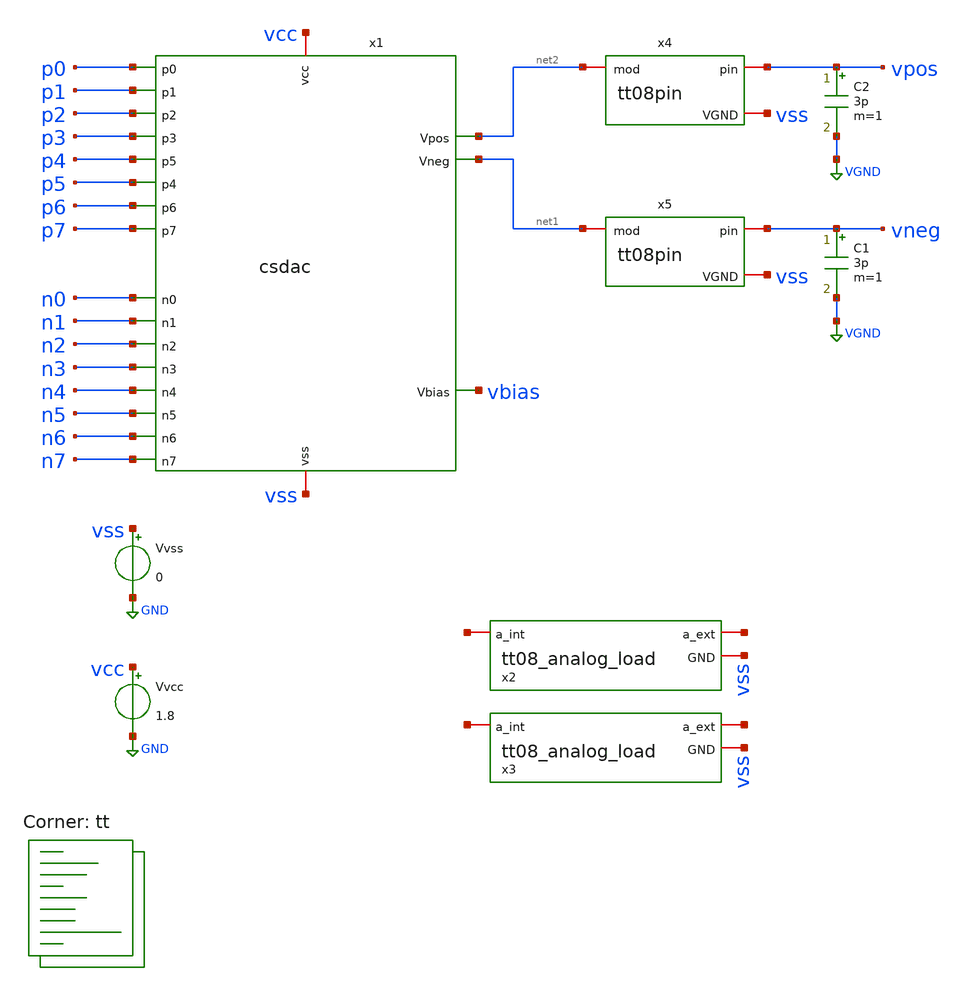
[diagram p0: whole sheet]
** sch_path: xschem/tb_csdac.sch
**.subckt tb_csdac
Vvcc vcc GND 1.8
Vvss vss GND 0
x1 vcc vss p0 p1 p2 p3 p4 p5 p6 p7 n0 n1 n2 n3 n4 n5 n6 n7 net2 net1 vbias csdac
x2 net3 net4 vss tt08_analog_load
x3 net5 net6 vss tt08_analog_load
x4 vpos net2 vss tt08pin
x5 vneg net1 vss tt08pin
C2 vpos VGND 3p m=1
C1 vneg VGND 3p m=1
**** begin user architecture code



* MPW:MMW=2.2:4.1 gets a linear range of 1V1..1V8 (0.7Vpp) with 2k5 pullups, uses ~600uA
* 4:4 is what I was using for original measurements: 0V736..1V8 (1.064Vpp); uses ~900uA
* 2:2 @ 2500R gets 0v733..1V8 (1.067Vpp) @ 650uA
* 0.5:0.5 @ 2500R gets 0v708..1v8 (1.092Vpp) @ ~500uA (Vbias around 1.373)
.param MPW=0.5
.param MMW=0.5

.param singlebits=0
.IF (singlebits == 1)
Vxp0 p0 GND pulse 0v 1.8v 1u 1n 1n 1u 10u
Vxp1 p1 GND pulse 0v 1.8v 2u 1n 1n 1u 10u
Vxp2 p2 GND pulse 0v 1.8v 3u 1n 1n 1u 10u
Vxp3 p3 GND pulse 0v 1.8v 4u 1n 1n 1u 10u
Vxp4 p4 GND pulse 0v 1.8v 5u 1n 1n 1u 10u
Vxp5 p5 GND pulse 0v 1.8v 6u 1n 1n 1u 10u
Vxp6 p6 GND pulse 0v 1.8v 7u 1n 1n 1u 10u
Vxp7 p7 GND pulse 0v 1.8v 8u 1n 1n 1u 10u
Vxn0 n0 GND pulse 1.8v 0v 1u 1n 1n 1u 10u
Vxn1 n1 GND pulse 1.8v 0v 2u 1n 1n 1u 10u
Vxn2 n2 GND pulse 1.8v 0v 3u 1n 1n 1u 10u
Vxn3 n3 GND pulse 1.8v 0v 4u 1n 1n 1u 10u
Vxn4 n4 GND pulse 1.8v 0v 5u 1n 1n 1u 10u
Vxn5 n5 GND pulse 1.8v 0v 6u 1n 1n 1u 10u
Vxn6 n6 GND pulse 1.8v 0v 7u 1n 1n 1u 10u
Vxn7 n7 GND pulse 1.8v 0v 8u 1n 1n 1u 10u
.ELSEIF (singlebits == 0)
Vxp0 p0 GND pulse 1.8v 0v 0n 1n 1n 39n 80n
Vxp1 p1 GND pulse 1.8v 0v 0n 1n 1n 79n 160n
Vxp2 p2 GND pulse 1.8v 0v 0n 1n 1n 159n 320n
Vxp3 p3 GND pulse 1.8v 0v 0n 1n 1n 319n 640n
Vxp4 p4 GND pulse 1.8v 0v 0n 1n 1n 639n 1280n
Vxp5 p5 GND pulse 1.8v 0v 0n 1n 1n 1279n 2560n
Vxp6 p6 GND pulse 1.8v 0v 0n 1n 1n 2559n 5120n
Vxp7 p7 GND pulse 1.8v 0v 0n 1n 1n 5119n 10240n
Vxn0 n0 GND pulse 0v 1.8v 0n 1n 1n 39n 80n
Vxn1 n1 GND pulse 0v 1.8v 0n 1n 1n 79n 160n
Vxn2 n2 GND pulse 0v 1.8v 0n 1n 1n 159n 320n
Vxn3 n3 GND pulse 0v 1.8v 0n 1n 1n 319n 640n
Vxn4 n4 GND pulse 0v 1.8v 0n 1n 1n 639n 1280n
Vxn5 n5 GND pulse 0v 1.8v 0n 1n 1n 1279n 2560n
Vxn6 n6 GND pulse 0v 1.8v 0n 1n 1n 2559n 5120n
Vxn7 n7 GND pulse 0v 1.8v 0n 1n 1n 5119n 10240n
.ENDIF

.options savecurrents
.control

  save all
  *reset
  *alterparam MPW=4
  *alterparam MMW=4
  tran 1n 12.8u
  write 11.raw i(vvcc) i(vvss) vpos vneg vbias

*  set appendwrite
*  alterparam MPW=4
*  alterparam MMW=4
*  reset
*  tran 1n 12.8u
*  write 11.raw i(vvcc) i(vvss) vpos vneg vbias

.endc



.lib $::SKYWATER_MODELS/sky130.lib.spice tt
**** end user architecture code
**.ends
.GLOBAL GND
.GLOBAL VGND
.end
